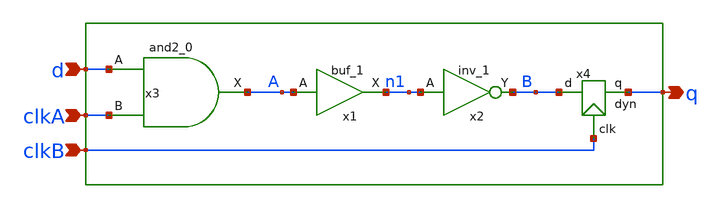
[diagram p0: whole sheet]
** sch_path: src/xe/test_cases/and_dyn_odd.sch
**.subckt and_dyn_odd d clkA q clkB
*.ipin d
*.ipin clkA
*.opin q
*.ipin clkB
x4 clkB q B dyn
x1 A vss vss vcc vcc n1 sky130_fd_sc_hd__buf_1
x3 d clkA vss vss vcc vcc A sky130_fd_sc_hd__and2_0
x2 n1 vss vss vcc vcc B sky130_fd_sc_hd__inv_1
**.ends

* expanding   symbol:  yxt/dyn.sym # of pins=3
** sym_path: src/xe/test_cases/dyn.sym
** sch_path: src/xe/test_cases/dyn.sch
.subckt dyn clk q d
*.ipin clk
*.opin q
*.ipin d
x1 z vss vss vcc vcc q sky130_fd_sc_hd__inv_1
XM1 z d net1 vss sky130_fd_pr__nfet_01v8 L=0.15 W=1 nf=1 ad='int((nf+1)/2) * W/nf * 0.29' as='int((nf+2)/2) * W/nf * 0.29'
+ pd='2*int((nf+1)/2) * (W/nf + 0.29)' ps='2*int((nf+2)/2) * (W/nf + 0.29)' nrd='0.29 / W' nrs='0.29 / W'
+ sa=0 sb=0 sd=0 mult=1 m=1
XM2 z q vcc vcc sky130_fd_pr__pfet_01v8 L=0.15 W=1 nf=1 ad='int((nf+1)/2) * W/nf * 0.29' as='int((nf+2)/2) * W/nf * 0.29'
+ pd='2*int((nf+1)/2) * (W/nf + 0.29)' ps='2*int((nf+2)/2) * (W/nf + 0.29)' nrd='0.29 / W' nrs='0.29 / W'
+ sa=0 sb=0 sd=0 mult=1 m=1
XM3 z clk vcc vcc sky130_fd_pr__pfet_01v8 L=0.15 W=1 nf=1 ad='int((nf+1)/2) * W/nf * 0.29' as='int((nf+2)/2) * W/nf * 0.29'
+ pd='2*int((nf+1)/2) * (W/nf + 0.29)' ps='2*int((nf+2)/2) * (W/nf + 0.29)' nrd='0.29 / W' nrs='0.29 / W'
+ sa=0 sb=0 sd=0 mult=1 m=1
XM4 net1 clk vss vss sky130_fd_pr__nfet_01v8 L=0.15 W=1 nf=1 ad='int((nf+1)/2) * W/nf * 0.29' as='int((nf+2)/2) * W/nf * 0.29'
+ pd='2*int((nf+1)/2) * (W/nf + 0.29)' ps='2*int((nf+2)/2) * (W/nf + 0.29)' nrd='0.29 / W' nrs='0.29 / W'
+ sa=0 sb=0 sd=0 mult=1 m=1
.ends

.end
